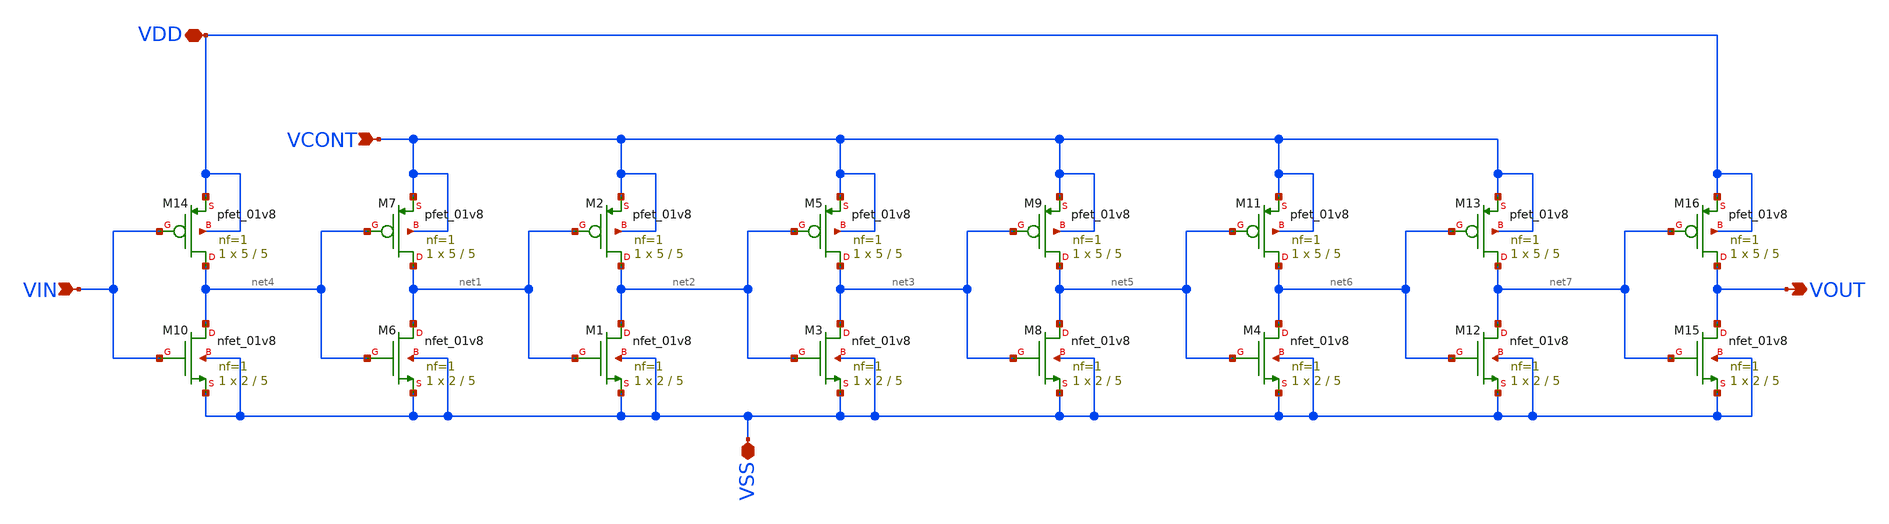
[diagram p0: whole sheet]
** sch_path: xschem/VCDL_Kim15_v2p1.sch
**.subckt VCDL_Kim15_v2p1 VIN VOUT VSS VCONT VDD
*.ipin VIN
*.opin VOUT
*.iopin VSS
*.ipin VCONT
*.iopin VDD
XM1 net2 net1 VSS VSS sky130_fd_pr__nfet_01v8 L=5 W=2 nf=1 ad='int((nf+1)/2) * W/nf * 0.29' as='int((nf+2)/2) * W/nf * 0.29'
+ pd='2*int((nf+1)/2) * (W/nf + 0.29)' ps='2*int((nf+2)/2) * (W/nf + 0.29)' nrd='0.29 / W' nrs='0.29 / W'
+ sa=0 sb=0 sd=0 mult=1 m=1
XM2 net2 net1 VCONT VCONT sky130_fd_pr__pfet_01v8 L=5 W=5 nf=1 ad='int((nf+1)/2) * W/nf * 0.29' as='int((nf+2)/2) * W/nf * 0.29'
+ pd='2*int((nf+1)/2) * (W/nf + 0.29)' ps='2*int((nf+2)/2) * (W/nf + 0.29)' nrd='0.29 / W' nrs='0.29 / W'
+ sa=0 sb=0 sd=0 mult=1 m=1
XM3 net3 net2 VSS VSS sky130_fd_pr__nfet_01v8 L=5 W=2 nf=1 ad='int((nf+1)/2) * W/nf * 0.29' as='int((nf+2)/2) * W/nf * 0.29'
+ pd='2*int((nf+1)/2) * (W/nf + 0.29)' ps='2*int((nf+2)/2) * (W/nf + 0.29)' nrd='0.29 / W' nrs='0.29 / W'
+ sa=0 sb=0 sd=0 mult=1 m=1
XM5 net3 net2 VCONT VCONT sky130_fd_pr__pfet_01v8 L=5 W=5 nf=1 ad='int((nf+1)/2) * W/nf * 0.29' as='int((nf+2)/2) * W/nf * 0.29'
+ pd='2*int((nf+1)/2) * (W/nf + 0.29)' ps='2*int((nf+2)/2) * (W/nf + 0.29)' nrd='0.29 / W' nrs='0.29 / W'
+ sa=0 sb=0 sd=0 mult=1 m=1
XM6 net1 net4 VSS VSS sky130_fd_pr__nfet_01v8 L=5 W=2 nf=1 ad='int((nf+1)/2) * W/nf * 0.29' as='int((nf+2)/2) * W/nf * 0.29'
+ pd='2*int((nf+1)/2) * (W/nf + 0.29)' ps='2*int((nf+2)/2) * (W/nf + 0.29)' nrd='0.29 / W' nrs='0.29 / W'
+ sa=0 sb=0 sd=0 mult=1 m=1
XM7 net1 net4 VCONT VCONT sky130_fd_pr__pfet_01v8 L=5 W=5 nf=1 ad='int((nf+1)/2) * W/nf * 0.29' as='int((nf+2)/2) * W/nf * 0.29'
+ pd='2*int((nf+1)/2) * (W/nf + 0.29)' ps='2*int((nf+2)/2) * (W/nf + 0.29)' nrd='0.29 / W' nrs='0.29 / W'
+ sa=0 sb=0 sd=0 mult=1 m=1
XM8 net5 net3 VSS VSS sky130_fd_pr__nfet_01v8 L=5 W=2 nf=1 ad='int((nf+1)/2) * W/nf * 0.29' as='int((nf+2)/2) * W/nf * 0.29'
+ pd='2*int((nf+1)/2) * (W/nf + 0.29)' ps='2*int((nf+2)/2) * (W/nf + 0.29)' nrd='0.29 / W' nrs='0.29 / W'
+ sa=0 sb=0 sd=0 mult=1 m=1
XM9 net5 net3 VCONT VCONT sky130_fd_pr__pfet_01v8 L=5 W=5 nf=1 ad='int((nf+1)/2) * W/nf * 0.29' as='int((nf+2)/2) * W/nf * 0.29'
+ pd='2*int((nf+1)/2) * (W/nf + 0.29)' ps='2*int((nf+2)/2) * (W/nf + 0.29)' nrd='0.29 / W' nrs='0.29 / W'
+ sa=0 sb=0 sd=0 mult=1 m=1
XM4 net6 net5 VSS VSS sky130_fd_pr__nfet_01v8 L=5 W=2 nf=1 ad='int((nf+1)/2) * W/nf * 0.29' as='int((nf+2)/2) * W/nf * 0.29'
+ pd='2*int((nf+1)/2) * (W/nf + 0.29)' ps='2*int((nf+2)/2) * (W/nf + 0.29)' nrd='0.29 / W' nrs='0.29 / W'
+ sa=0 sb=0 sd=0 mult=1 m=1
XM11 net6 net5 VCONT VCONT sky130_fd_pr__pfet_01v8 L=5 W=5 nf=1 ad='int((nf+1)/2) * W/nf * 0.29' as='int((nf+2)/2) * W/nf * 0.29'
+ pd='2*int((nf+1)/2) * (W/nf + 0.29)' ps='2*int((nf+2)/2) * (W/nf + 0.29)' nrd='0.29 / W' nrs='0.29 / W'
+ sa=0 sb=0 sd=0 mult=1 m=1
XM12 net7 net6 VSS VSS sky130_fd_pr__nfet_01v8 L=5 W=2 nf=1 ad='int((nf+1)/2) * W/nf * 0.29' as='int((nf+2)/2) * W/nf * 0.29'
+ pd='2*int((nf+1)/2) * (W/nf + 0.29)' ps='2*int((nf+2)/2) * (W/nf + 0.29)' nrd='0.29 / W' nrs='0.29 / W'
+ sa=0 sb=0 sd=0 mult=1 m=1
XM13 net7 net6 VCONT VCONT sky130_fd_pr__pfet_01v8 L=5 W=5 nf=1 ad='int((nf+1)/2) * W/nf * 0.29' as='int((nf+2)/2) * W/nf * 0.29'
+ pd='2*int((nf+1)/2) * (W/nf + 0.29)' ps='2*int((nf+2)/2) * (W/nf + 0.29)' nrd='0.29 / W' nrs='0.29 / W'
+ sa=0 sb=0 sd=0 mult=1 m=1
XM10 net4 VIN VSS VSS sky130_fd_pr__nfet_01v8 L=5 W=2 nf=1 ad='int((nf+1)/2) * W/nf * 0.29' as='int((nf+2)/2) * W/nf * 0.29'
+ pd='2*int((nf+1)/2) * (W/nf + 0.29)' ps='2*int((nf+2)/2) * (W/nf + 0.29)' nrd='0.29 / W' nrs='0.29 / W'
+ sa=0 sb=0 sd=0 mult=1 m=1
XM14 net4 VIN VDD VDD sky130_fd_pr__pfet_01v8 L=5 W=5 nf=1 ad='int((nf+1)/2) * W/nf * 0.29' as='int((nf+2)/2) * W/nf * 0.29'
+ pd='2*int((nf+1)/2) * (W/nf + 0.29)' ps='2*int((nf+2)/2) * (W/nf + 0.29)' nrd='0.29 / W' nrs='0.29 / W'
+ sa=0 sb=0 sd=0 mult=1 m=1
XM15 VOUT net7 VSS VSS sky130_fd_pr__nfet_01v8 L=5 W=2 nf=1 ad='int((nf+1)/2) * W/nf * 0.29' as='int((nf+2)/2) * W/nf * 0.29'
+ pd='2*int((nf+1)/2) * (W/nf + 0.29)' ps='2*int((nf+2)/2) * (W/nf + 0.29)' nrd='0.29 / W' nrs='0.29 / W'
+ sa=0 sb=0 sd=0 mult=1 m=1
XM16 VOUT net7 VDD VDD sky130_fd_pr__pfet_01v8 L=5 W=5 nf=1 ad='int((nf+1)/2) * W/nf * 0.29' as='int((nf+2)/2) * W/nf * 0.29'
+ pd='2*int((nf+1)/2) * (W/nf + 0.29)' ps='2*int((nf+2)/2) * (W/nf + 0.29)' nrd='0.29 / W' nrs='0.29 / W'
+ sa=0 sb=0 sd=0 mult=1 m=1
**.ends
.end
